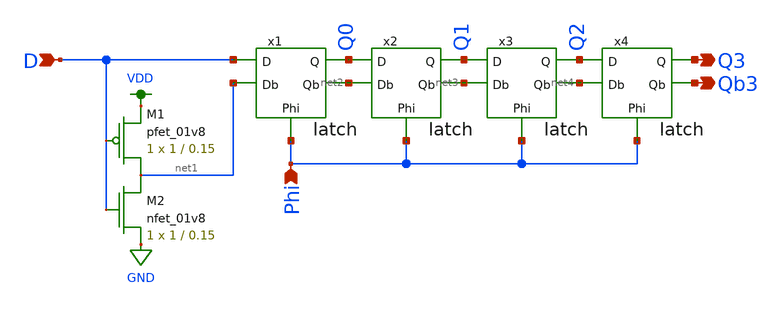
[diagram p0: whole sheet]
** sch_path: mp2/sr.sch
**.subckt sr Phi D Q3 Qb3
*.ipin Phi
*.ipin D
*.opin Q3
*.opin Qb3
x1 D Q0 net1 net2 Phi latch
x2 Q0 Q1 net2 net3 Phi latch
x3 Q1 Q2 net3 net4 Phi latch
x4 Q2 Q3 net4 Qb3 Phi latch
XM1 net1 D VDD VDD sky130_fd_pr__pfet_01v8 L=0.15 W=1 nf=1 ad='int((nf+1)/2) * W/nf * 0.29' as='int((nf+2)/2) * W/nf * 0.29'
+ pd='2*int((nf+1)/2) * (W/nf + 0.29)' ps='2*int((nf+2)/2) * (W/nf + 0.29)' nrd='0.29 / W' nrs='0.29 / W'
+ sa=0 sb=0 sd=0 mult=1 m=1
XM2 net1 D GND GND sky130_fd_pr__nfet_01v8 L=0.15 W=1 nf=1 ad='int((nf+1)/2) * W/nf * 0.29' as='int((nf+2)/2) * W/nf * 0.29'
+ pd='2*int((nf+1)/2) * (W/nf + 0.29)' ps='2*int((nf+2)/2) * (W/nf + 0.29)' nrd='0.29 / W' nrs='0.29 / W'
+ sa=0 sb=0 sd=0 mult=1 m=1
**.ends

* expanding   symbol:  /home/madvlsi/Documents/mp2/latch.sym # of pins=5
** sym_path: mp2/latch.sym
** sch_path: mp2/latch.sch
.subckt latch D Q Db Qb Phi
*.ipin D
*.ipin Db
*.opin Q
*.opin Qb
*.ipin Phi
XM1 net1 net2 VDD VDD sky130_fd_pr__pfet_01v8 L=0.15 W=1 nf=1 ad='int((nf+1)/2) * W/nf * 0.29' as='int((nf+2)/2) * W/nf * 0.29'
+ pd='2*int((nf+1)/2) * (W/nf + 0.29)' ps='2*int((nf+2)/2) * (W/nf + 0.29)' nrd='0.29 / W' nrs='0.29 / W'
+ sa=0 sb=0 sd=0 mult=1 m=1
XM2 net2 net1 VDD VDD sky130_fd_pr__pfet_01v8 L=0.15 W=1 nf=1 ad='int((nf+1)/2) * W/nf * 0.29' as='int((nf+2)/2) * W/nf * 0.29'
+ pd='2*int((nf+1)/2) * (W/nf + 0.29)' ps='2*int((nf+2)/2) * (W/nf + 0.29)' nrd='0.29 / W' nrs='0.29 / W'
+ sa=0 sb=0 sd=0 mult=1 m=1
XM3 net3 net2 net1 GND sky130_fd_pr__nfet_01v8 L=0.15 W=1 nf=1 ad='int((nf+1)/2) * W/nf * 0.29' as='int((nf+2)/2) * W/nf * 0.29'
+ pd='2*int((nf+1)/2) * (W/nf + 0.29)' ps='2*int((nf+2)/2) * (W/nf + 0.29)' nrd='0.29 / W' nrs='0.29 / W'
+ sa=0 sb=0 sd=0 mult=1 m=1
XM4 net3 net1 net2 GND sky130_fd_pr__nfet_01v8 L=0.15 W=1 nf=1 ad='int((nf+1)/2) * W/nf * 0.29' as='int((nf+2)/2) * W/nf * 0.29'
+ pd='2*int((nf+1)/2) * (W/nf + 0.29)' ps='2*int((nf+2)/2) * (W/nf + 0.29)' nrd='0.29 / W' nrs='0.29 / W'
+ sa=0 sb=0 sd=0 mult=1 m=1
XM5 net3 Phi GND GND sky130_fd_pr__nfet_01v8 L=0.15 W=4.01 nf=1 ad='int((nf+1)/2) * W/nf * 0.29' as='int((nf+2)/2) * W/nf * 0.29'
+ pd='2*int((nf+1)/2) * (W/nf + 0.29)' ps='2*int((nf+2)/2) * (W/nf + 0.29)' nrd='0.29 / W' nrs='0.29 / W'
+ sa=0 sb=0 sd=0 mult=1 m=1
XM6 net1 Phi Db VDD sky130_fd_pr__pfet_01v8 L=0.15 W=1 nf=1 ad='int((nf+1)/2) * W/nf * 0.29' as='int((nf+2)/2) * W/nf * 0.29'
+ pd='2*int((nf+1)/2) * (W/nf + 0.29)' ps='2*int((nf+2)/2) * (W/nf + 0.29)' nrd='0.29 / W' nrs='0.29 / W'
+ sa=0 sb=0 sd=0 mult=1 m=1
XM7 net2 Phi D VDD sky130_fd_pr__pfet_01v8 L=0.15 W=1 nf=1 ad='int((nf+1)/2) * W/nf * 0.29' as='int((nf+2)/2) * W/nf * 0.29'
+ pd='2*int((nf+1)/2) * (W/nf + 0.29)' ps='2*int((nf+2)/2) * (W/nf + 0.29)' nrd='0.29 / W' nrs='0.29 / W'
+ sa=0 sb=0 sd=0 mult=1 m=1
XM8 Qb Q net4 VDD sky130_fd_pr__pfet_01v8 L=0.15 W=1 nf=1 ad='int((nf+1)/2) * W/nf * 0.29' as='int((nf+2)/2) * W/nf * 0.29'
+ pd='2*int((nf+1)/2) * (W/nf + 0.29)' ps='2*int((nf+2)/2) * (W/nf + 0.29)' nrd='0.29 / W' nrs='0.29 / W'
+ sa=0 sb=0 sd=0 mult=1 m=1
XM9 Q Qb net4 VDD sky130_fd_pr__pfet_01v8 L=0.15 W=1 nf=1 ad='int((nf+1)/2) * W/nf * 0.29' as='int((nf+2)/2) * W/nf * 0.29'
+ pd='2*int((nf+1)/2) * (W/nf + 0.29)' ps='2*int((nf+2)/2) * (W/nf + 0.29)' nrd='0.29 / W' nrs='0.29 / W'
+ sa=0 sb=0 sd=0 mult=1 m=1
XM10 Qb Q GND GND sky130_fd_pr__nfet_01v8 L=0.15 W=1 nf=1 ad='int((nf+1)/2) * W/nf * 0.29' as='int((nf+2)/2) * W/nf * 0.29'
+ pd='2*int((nf+1)/2) * (W/nf + 0.29)' ps='2*int((nf+2)/2) * (W/nf + 0.29)' nrd='0.29 / W' nrs='0.29 / W'
+ sa=0 sb=0 sd=0 mult=1 m=1
XM11 Q Qb GND GND sky130_fd_pr__nfet_01v8 L=0.15 W=1 nf=1 ad='int((nf+1)/2) * W/nf * 0.29' as='int((nf+2)/2) * W/nf * 0.29'
+ pd='2*int((nf+1)/2) * (W/nf + 0.29)' ps='2*int((nf+2)/2) * (W/nf + 0.29)' nrd='0.29 / W' nrs='0.29 / W'
+ sa=0 sb=0 sd=0 mult=1 m=1
XM12 Qb Phi net1 GND sky130_fd_pr__nfet_01v8 L=0.15 W=1 nf=1 ad='int((nf+1)/2) * W/nf * 0.29' as='int((nf+2)/2) * W/nf * 0.29'
+ pd='2*int((nf+1)/2) * (W/nf + 0.29)' ps='2*int((nf+2)/2) * (W/nf + 0.29)' nrd='0.29 / W' nrs='0.29 / W'
+ sa=0 sb=0 sd=0 mult=1 m=1
XM13 Q Phi net2 GND sky130_fd_pr__nfet_01v8 L=0.15 W=1 nf=1 ad='int((nf+1)/2) * W/nf * 0.29' as='int((nf+2)/2) * W/nf * 0.29'
+ pd='2*int((nf+1)/2) * (W/nf + 0.29)' ps='2*int((nf+2)/2) * (W/nf + 0.29)' nrd='0.29 / W' nrs='0.29 / W'
+ sa=0 sb=0 sd=0 mult=1 m=1
XM14 net4 Phi VDD VDD sky130_fd_pr__pfet_01v8 L=0.15 W=4.01 nf=1 ad='int((nf+1)/2) * W/nf * 0.29' as='int((nf+2)/2) * W/nf * 0.29'
+ pd='2*int((nf+1)/2) * (W/nf + 0.29)' ps='2*int((nf+2)/2) * (W/nf + 0.29)' nrd='0.29 / W' nrs='0.29 / W'
+ sa=0 sb=0 sd=0 mult=1 m=1
.ends

.GLOBAL VDD
.GLOBAL GND
.end
